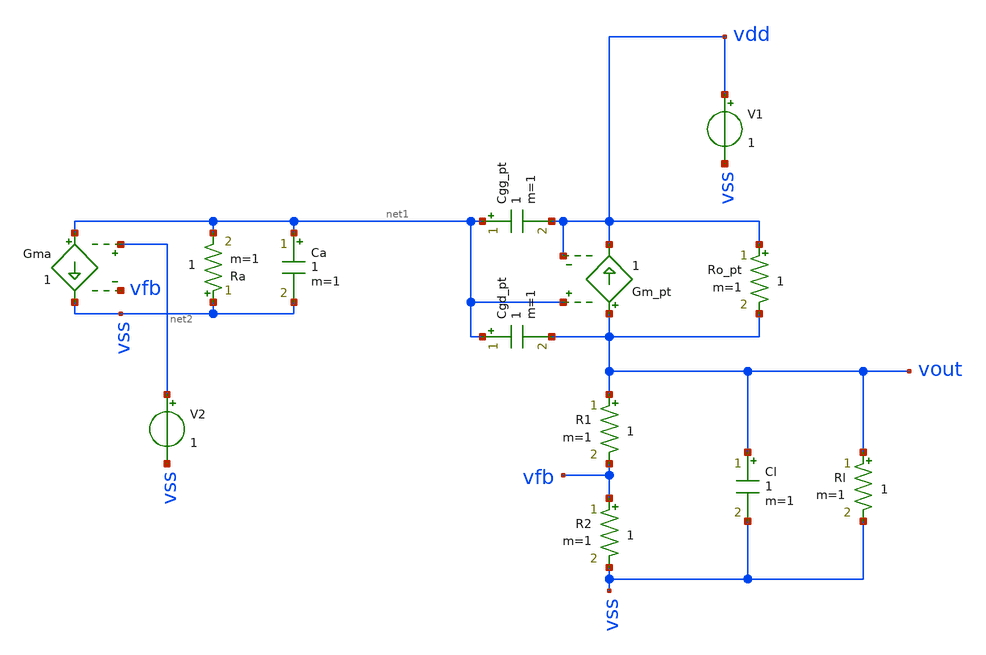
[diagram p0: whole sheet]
** sch_path: test/Tesis_notebooks/xschem/ldo.sch
**.subckt ldo
Ro_pt vdd vout 1 m=1
Gm_pt vout vdd net1 vdd 1
R1 vout vfb 1 m=1
R2 vfb vss 1 m=1
Gma net1 vss net2 vfb 1
Ra vss net1 1 m=1
V1 vdd vss 1
Rl vout vss 1 m=1
Cgg_pt net1 vdd 1 m=1
Cgd_pt net1 vout 1 m=1
Ca net1 vss 1 m=1
Cl vout vss 1 m=1
V2 net2 vss 1
**.ends
.end
